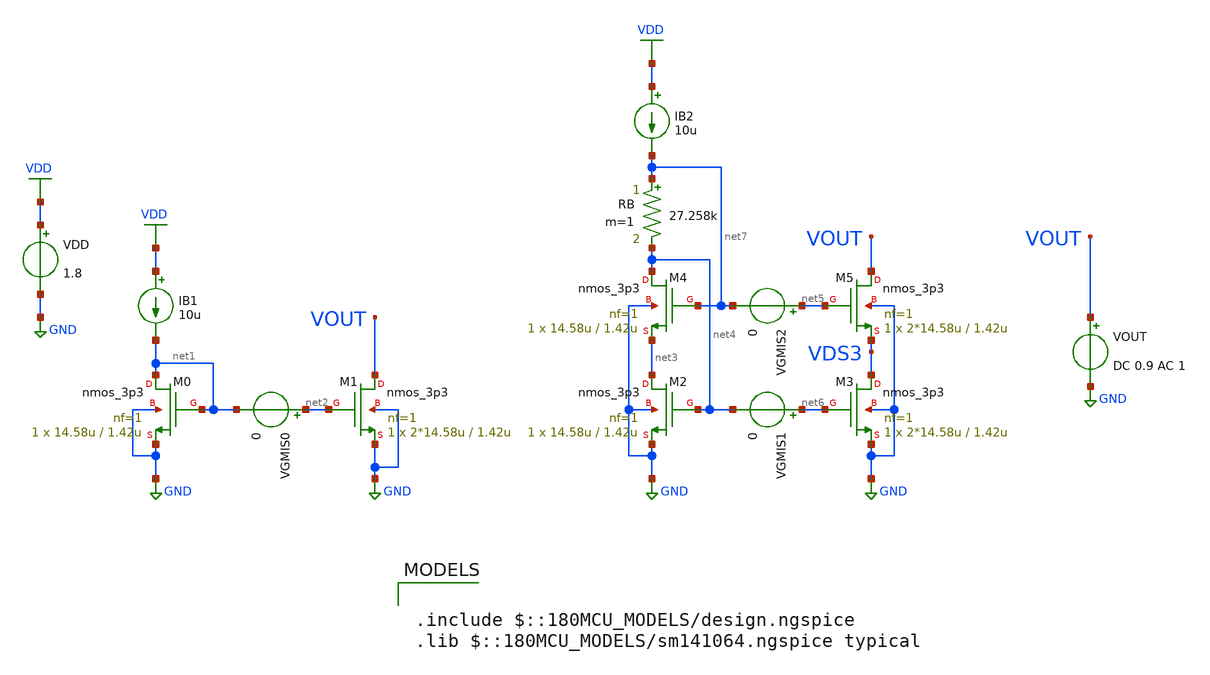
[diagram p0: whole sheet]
** sch_path: ITI_Labs/Lab5/Design/Lab5.sch
**.subckt Lab5
XM0 net1 net1 GND GND nmos_3p3 L=1.42u W=14.58u nf=1 ad='int((nf+1)/2) * W/nf * 0.18u' as='int((nf+2)/2) * W/nf * 0.18u'
+ pd='2*int((nf+1)/2) * (W/nf + 0.18u)' ps='2*int((nf+2)/2) * (W/nf + 0.18u)' nrd='0.18u / W' nrs='0.18u / W'
+ sa=0 sb=0 sd=0 m=1
VDD VDD GND 1.8
IB1 VDD net1 10u
VGMIS0 net2 net1 0
RB net7 net4 27.258k m=1
XM1 VOUT net2 GND GND nmos_3p3 L=1.42u W=2*14.58u nf=1 ad='int((nf+1)/2) * W/nf * 0.18u' as='int((nf+2)/2) * W/nf * 0.18u'
+ pd='2*int((nf+1)/2) * (W/nf + 0.18u)' ps='2*int((nf+2)/2) * (W/nf + 0.18u)' nrd='0.18u / W' nrs='0.18u / W'
+ sa=0 sb=0 sd=0 m=1
IB2 VDD net7 10u
XM2 net3 net4 GND GND nmos_3p3 L=1.42u W=14.58u nf=1 ad='int((nf+1)/2) * W/nf * 0.18u' as='int((nf+2)/2) * W/nf * 0.18u'
+ pd='2*int((nf+1)/2) * (W/nf + 0.18u)' ps='2*int((nf+2)/2) * (W/nf + 0.18u)' nrd='0.18u / W' nrs='0.18u / W'
+ sa=0 sb=0 sd=0 m=1
XM3 VDS3 net6 GND GND nmos_3p3 L=1.42u W=2*14.58u nf=1 ad='int((nf+1)/2) * W/nf * 0.18u' as='int((nf+2)/2) * W/nf * 0.18u'
+ pd='2*int((nf+1)/2) * (W/nf + 0.18u)' ps='2*int((nf+2)/2) * (W/nf + 0.18u)' nrd='0.18u / W' nrs='0.18u / W'
+ sa=0 sb=0 sd=0 m=1
XM4 net4 net7 net3 GND nmos_3p3 L=1.42u W=14.58u nf=1 ad='int((nf+1)/2) * W/nf * 0.18u' as='int((nf+2)/2) * W/nf * 0.18u'
+ pd='2*int((nf+1)/2) * (W/nf + 0.18u)' ps='2*int((nf+2)/2) * (W/nf + 0.18u)' nrd='0.18u / W' nrs='0.18u / W'
+ sa=0 sb=0 sd=0 m=1
XM5 VOUT net5 VDS3 GND nmos_3p3 L=1.42u W=2*14.58u nf=1 ad='int((nf+1)/2) * W/nf * 0.18u' as='int((nf+2)/2) * W/nf * 0.18u'
+ pd='2*int((nf+1)/2) * (W/nf + 0.18u)' ps='2*int((nf+2)/2) * (W/nf + 0.18u)' nrd='0.18u / W' nrs='0.18u / W'
+ sa=0 sb=0 sd=0 m=1
VGMIS1 net6 net4 0
VGMIS2 net5 net7 0
VOUT VOUT GND DC 0.9 AC 1
**** begin user architecture code


.include sim_script.sim



.include $::180MCU_MODELS/design.ngspice
.lib $::180MCU_MODELS/sm141064.ngspice typical

**** end user architecture code
**.ends
.GLOBAL VDD
.GLOBAL GND
.end
